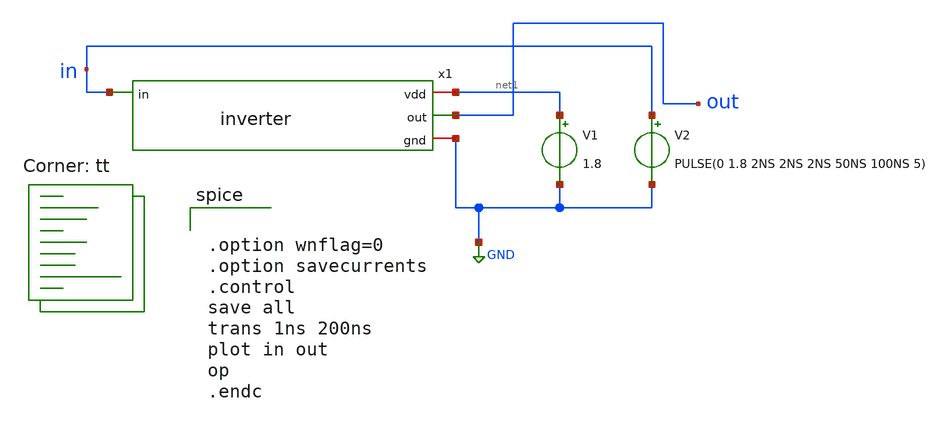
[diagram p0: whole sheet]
** sch_path: inverter_tb.sch
**.subckt inverter_tb
V1 net1 GND 1.8
V2 in GND PULSE(0 1.8 2NS 2NS 2NS 50NS 100NS 5)
x1 net1 in out GND inverter
**** begin user architecture code


.option wnflag=0
.option savecurrents
.control
save all
trans 1ns 200ns
plot in out
op
.endc


 .lib $::SKYWATER_MODELS/models/sky130.lib.spice tt
.param mc_mm_switch=0
.param mc_pr_switch=1

**** end user architecture code
**.ends

* expanding   symbol:  /home/mona121130125/percobaan_layout/inverter.sym # of pins=4
** sym_path: inverter.sym
** sch_path: inverter.sch
.subckt inverter vdd in out gnd
*.ipin in
*.opin out
*.iopin vdd
*.iopin gnd
XM1 out in vdd vdd sky130_fd_pr__pfet_01v8 L=0.15 W=1 nf=1 ad='int((nf+1)/2) * W/nf * 0.29' as='int((nf+2)/2) * W/nf * 0.29'
+ pd='2*int((nf+1)/2) * (W/nf + 0.29)' ps='2*int((nf+2)/2) * (W/nf + 0.29)' nrd='0.29 / W' nrs='0.29 / W'
+ sa=0 sb=0 sd=0 mult=1 m=1
XM2 out in gnd gnd sky130_fd_pr__nfet_01v8 L=0.15 W=1 nf=1 ad='int((nf+1)/2) * W/nf * 0.29' as='int((nf+2)/2) * W/nf * 0.29'
+ pd='2*int((nf+1)/2) * (W/nf + 0.29)' ps='2*int((nf+2)/2) * (W/nf + 0.29)' nrd='0.29 / W' nrs='0.29 / W'
+ sa=0 sb=0 sd=0 mult=1 m=1
.ends

.GLOBAL GND
.end
